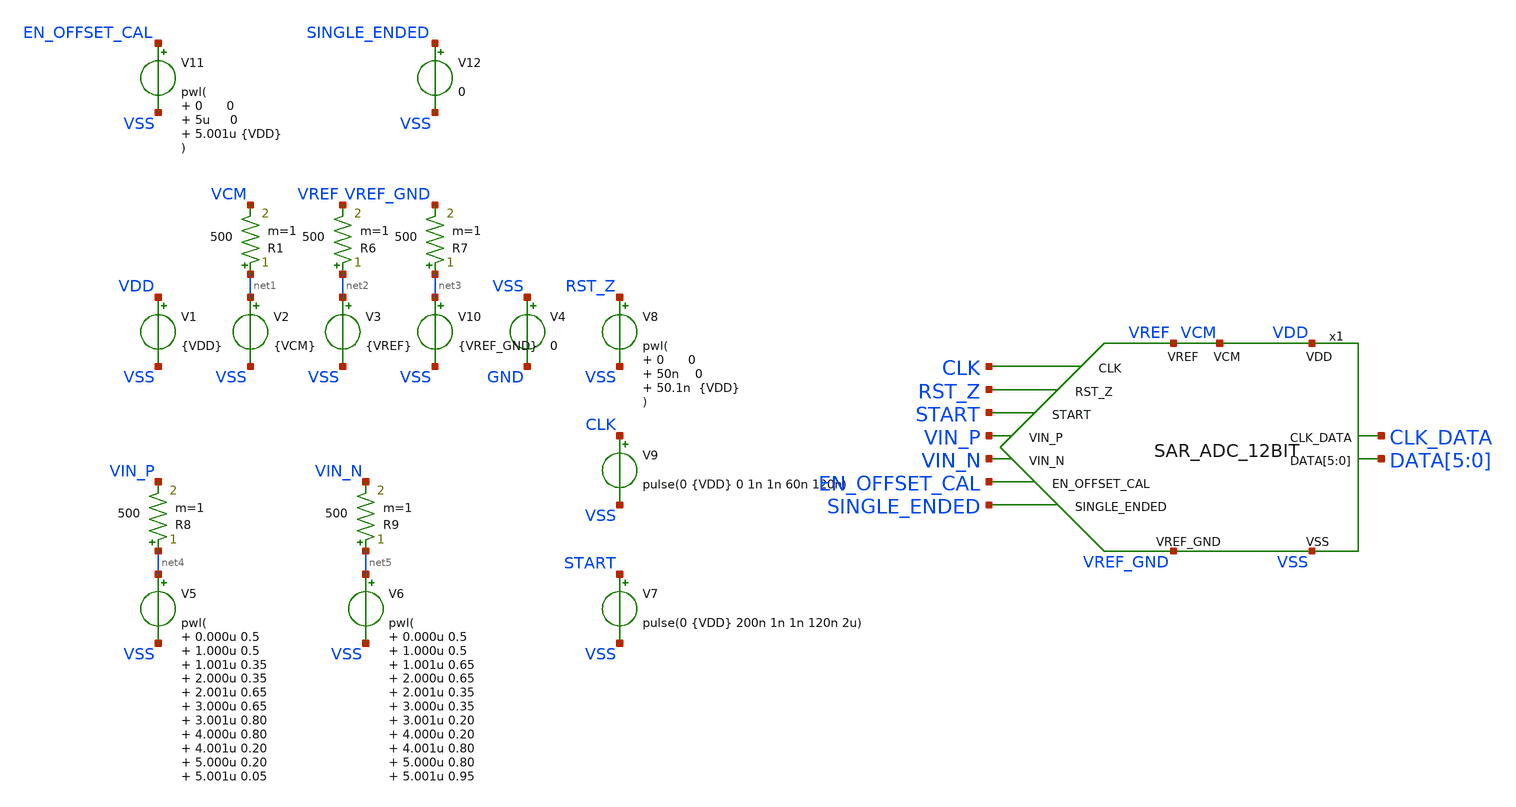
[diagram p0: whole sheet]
** sch_path: schematic/top_level_differential_sim1.sch
* IHP-GmbH/IHP-Open-PDK/ihp-sg13g2/libs.tech/xschem/sg13g2_stdcells/sg13g2_and3_1.sch:
* Copyright 2023 IHP PDK Authors
* Licensed under the Apache License, Version 2.0 (the "License");


* Models for standard digital cells
.include $PDK_ROOT/ihp-sg13g2/libs.ref/sg13g2_stdcell/spice/sg13g2_stdcell.spice

* Spice netlist for state machine generated by openlane
.include $HOME/SAR_ADC_12bit_ihp/schematic/state_machine/state_machine.spice

**.subckt top_level_differential_sim1
x1 VDD VCM VSS VREF VIN_P VIN_N RST_Z CLK_DATA DATA[5] DATA[4] DATA[3] DATA[2] DATA[1] DATA[0] START
+ EN_OFFSET_CAL CLK VREF_GND SINGLE_ENDED SAR_ADC_12BIT
V1 VDD VSS {VDD}
.save i(v1)
V2 net1 VSS {VCM}
.save i(v2)
V3 net2 VSS {VREF}
.save i(v3)
V4 VSS GND 0
V7 START VSS pulse(0 {VDD} 200n 1n 1n 120n 2u)
V8 RST_Z VSS pwl( 0 0 50n 0 50.1n {VDD}
)
V5 net4 VSS pwl( 0.000u 0.5 1.000u 0.5 1.001u 0.35 2.000u 0.35 2.001u 0.65 3.000u 0.65 3.001u 0.80
+ 4.000u 0.80 4.001u 0.20 5.000u 0.20 5.001u 0.05 6.000u 0.05 6.001u 0.95 7.000u 0.95
)
R1 net1 VCM 500 m=1
V9 CLK VSS pulse(0 {VDD} 0 1n 1n 60n 120n)
V6 net5 VSS pwl( 0.000u 0.5 1.000u 0.5 1.001u 0.65 2.000u 0.65 2.001u 0.35 3.000u 0.35 3.001u 0.20
+ 4.000u 0.20 4.001u 0.80 5.000u 0.80 5.001u 0.95 6.000u 0.95 6.001u 0.05 7.000u 0.05
)
V10 net3 VSS {VREF_GND}
.save i(v10)
R6 net2 VREF 500 m=1
R7 net3 VREF_GND 500 m=1
R8 net4 VIN_P 500 m=1
R9 net5 VIN_N 500 m=1
V11 EN_OFFSET_CAL VSS pwl( 0 0 5u 0 5.001u {VDD}
)
V12 SINGLE_ENDED VSS 0
**** begin user architecture code


* Supply, common mode and reference voltage
.param VDD = 1.2
.param VREF = 1
.param VREF_GND = 0
.param VCM = 0.5

.option temp = 27

*.save all

* Control signals
.save start rst_z clk en_offset_cal

* Input signals
.save vin_p vin_n

* Reference, supply
.save vref vref_gnd vcm vdd

* Output signals
.save clk_data data[5] data[4] data[3] data[2] data[1] data[0]

* Internal signals
.save x1.vdac_p x1.vdac_n x1.vdac_pi x1.vdac_ni x1.smpl x1.en_comp x1.comp_p x1.comp_n x1.cal_p x1.cal_n
.save x1.en_vin_bstr_p x1.en_vin_bstr_n
.save x1.c10_p_btm x1.c9_p_btm x1.c8_p_btm x1.c7_p_btm x1.c6_p_btm x1.c5_p_btm x1.c4_p_btm x1.c3_p_btm x1.c2_p_btm x1.c1_p_btm x1.c0_p_btm x1.C0_dummy_p_btm
.save x1.c10_n_btm x1.c9_n_btm x1.c8_n_btm x1.c7_n_btm x1.c6_n_btm x1.c5_n_btm x1.c4_n_btm x1.c3_n_btm x1.c2_n_btm x1.c1_n_btm x1.c0_n_btm x1.C0_dummy_n_btm

.option GMIN=1e-12 reltol=1e-5
.control
		set ngbehavior=hsa
          	set ng_nomodcheck
  		set num_threads=4
  		option noinit
  		option klu
		tran 10n 8u
		write top_level_differential_sim1.raw
.endc


**** end user architecture code
**.ends

* expanding   symbol:  SAR_ADC_12BIT.sym # of pins=14
** sym_path: schematic/SAR_ADC_12BIT.sym
** sch_path: schematic/SAR_ADC_12BIT.sch
.subckt SAR_ADC_12BIT VDD VCM VSS VREF VIN_P VIN_N RST_Z CLK_DATA DATA[5] DATA[4] DATA[3] DATA[2]
+ DATA[1] DATA[0] START EN_OFFSET_CAL CLK VREF_GND SINGLE_ENDED
*.ipin VIN_P
*.ipin VDD
*.ipin VREF
*.ipin VCM
*.ipin VSS
*.ipin VIN_N
*.ipin RST_Z
*.ipin START
*.opin CLK_DATA
*.opin DATA[5],DATA[4],DATA[3],DATA[2],DATA[1],DATA[0]
*.ipin EN_OFFSET_CAL
*.ipin CLK
*.ipin VREF_GND
*.ipin SINGLE_ENDED
x1 VDD VDAC_Pi VDAC_Ni COMP_P EN_COMP COMP_N VSS latched_comparator
x2 VDD COMP_P EN_COMP CAL_P CAL_N EN_VOS_CAL VSS OFFSET_CAL_CYCLE offset_calibration-1
x3 VDAC_N VDAC_P VDD RST_Z VDAC_Pi VDAC_Ni VSS CAL_P CAL_N preamplifier
x4 VCM VREF_GND VREF VIN_P EN_VIN_BSTR_P EN_REF_Z_P[10] EN_REF_Z_P[9] EN_REF_Z_P[8] EN_REF_Z_P[7]
+ EN_REF_Z_P[6] EN_REF_Z_P[5] EN_REF_Z_P[4] EN_REF_Z_P[3] EN_REF_Z_P[2] EN_REF_Z_P[1] EN_REF_Z_P[0] EN_VSS_P[10]
+ EN_VSS_P[9] EN_VSS_P[8] EN_VSS_P[7] EN_VSS_P[6] EN_VSS_P[5] EN_VSS_P[4] EN_VSS_P[3] EN_VSS_P[2] EN_VSS_P[1]
+ EN_VSS_P[0] EN_VCM[10] EN_VCM[9] EN_VCM[8] EN_VCM[7] EN_VCM[6] EN_VCM[5] EN_VCM[4] EN_VCM[3] EN_VCM[2]
+ EN_VCM[1] EN_VCM[0] EN_VCM_SW EN_VCM_DUMMY C8_P_btm C7_P_btm C0_P_btm C6_P_btm C5_P_btm C0_dummy_P_btm
+ C4_P_btm C3_P_btm VDAC_P C10_P_btm C9_P_btm C2_P_btm C1_P_btm VDD VSS switches
x5 VCM VREF_GND VREF VIN_N EN_VIN_BSTR_N EN_REF_Z_N[10] EN_REF_Z_N[9] EN_REF_Z_N[8] EN_REF_Z_N[7]
+ EN_REF_Z_N[6] EN_REF_Z_N[5] EN_REF_Z_N[4] EN_REF_Z_N[3] EN_REF_Z_N[2] EN_REF_Z_N[1] EN_REF_Z_N[0] EN_VSS_N[10]
+ EN_VSS_N[9] EN_VSS_N[8] EN_VSS_N[7] EN_VSS_N[6] EN_VSS_N[5] EN_VSS_N[4] EN_VSS_N[3] EN_VSS_N[2] EN_VSS_N[1]
+ EN_VSS_N[0] EN_VCM[10] EN_VCM[9] EN_VCM[8] EN_VCM[7] EN_VCM[6] EN_VCM[5] EN_VCM[4] EN_VCM[3] EN_VCM[2]
+ EN_VCM[1] EN_VCM[0] EN_VCM_SW EN_VCM_DUMMY C8_N_btm C7_N_btm C0_N_btm C6_N_btm C5_N_btm C0_dummy_N_btm
+ C4_N_btm C3_N_btm VDAC_N C10_N_btm C9_N_btm C2_N_btm C1_N_btm VDD VSS switches
x8 EN_VSS_P_BBM[10] EN_VSS_P_BBM[9] EN_VSS_P_BBM[8] EN_VSS_P_BBM[7] EN_VSS_P_BBM[6] EN_VSS_P_BBM[5]
+ EN_VSS_P_BBM[4] EN_VSS_P_BBM[3] EN_VSS_P_BBM[2] EN_VSS_P_BBM[1] EN_VSS_P_BBM[0] VDD VSS EN_VSS_P[10] EN_VSS_P[9]
+ EN_VSS_P[8] EN_VSS_P[7] EN_VSS_P[6] EN_VSS_P[5] EN_VSS_P[4] EN_VSS_P[3] EN_VSS_P[2] EN_VSS_P[1] EN_VSS_P[0]
+ EN_REF_Z_P[10] EN_REF_Z_P[9] EN_REF_Z_P[8] EN_REF_Z_P[7] EN_REF_Z_P[6] EN_REF_Z_P[5] EN_REF_Z_P[4] EN_REF_Z_P[3]
+ EN_REF_Z_P[2] EN_REF_Z_P[1] EN_REF_Z_P[0] EN_REF_Z_P_BBM[10] EN_REF_Z_P_BBM[9] EN_REF_Z_P_BBM[8]
+ EN_REF_Z_P_BBM[7] EN_REF_Z_P_BBM[6] EN_REF_Z_P_BBM[5] EN_REF_Z_P_BBM[4] EN_REF_Z_P_BBM[3] EN_REF_Z_P_BBM[2]
+ EN_REF_Z_P_BBM[1] EN_REF_Z_P_BBM[0] break_before_make
x9 VDD EN_VIN_BSTR_P VSS SMPL_ON_P VIN_P SMPL bootstrap
x10 VDD EN_VIN_BSTR_N VSS SMPL_ON_N VIN_N SMPL bootstrap
C0_dummy C0_dummy_P_btm VDAC_P 10f m=1
C0 C0_P_btm VDAC_P 10f m=1
C1 C1_P_btm VDAC_P 20f m=1
C2 C2_P_btm VDAC_P 40f m=1
C3 C3_P_btm VDAC_P 80f m=1
C4 C4_P_btm VDAC_P 160f m=1
C5 C5_P_btm VDAC_P 320f m=1
C6 C6_P_btm VDAC_P 640f m=1
C7 C7_P_btm VDAC_P 1.28p m=1
C8 C8_P_btm VDAC_P 2.56p m=1
C9 C9_P_btm VDAC_P 5.12p m=1
C10 C10_P_btm VDAC_P 10.24p m=1
C11 VSS VDAC_P 20.48p m=1
C12 VDAC_N C0_dummy_N_btm 10f m=1
C13 VDAC_N C0_N_btm 10f m=1
C14 VDAC_N C1_N_btm 20f m=1
C15 VDAC_N C2_N_btm 40f m=1
C16 VDAC_N C3_N_btm 80f m=1
C17 VDAC_N C4_N_btm 160f m=1
C18 VDAC_N C5_N_btm 320f m=1
C19 VDAC_N C6_N_btm 640f m=1
C20 VDAC_N C7_N_btm 1.28p m=1
C21 VDAC_N C8_N_btm 2.56p m=1
C22 VDAC_N C9_N_btm 5.12p m=1
C23 VDAC_N C10_N_btm 10.24p m=1
C24 VDAC_N VSS 20.48p m=1
.ends


* expanding   symbol:  latched_comparator/latched_comparator.sym # of pins=7
** sym_path: schematic/latched_comparator/latched_comparator.sym
** sch_path: schematic/latched_comparator/latched_comparator.sch
.subckt latched_comparator VDD Vin_P Vin_N OUT_P EN OUT_N VSS
*.ipin Vin_P
*.ipin Vin_N
*.iopin VDD
*.iopin VSS
*.ipin EN
*.opin OUT_P
*.opin OUT_N
XM1 net1 ENi VDD VDD sg13_lv_pmos w=0.32u l=0.15u ng=1 m=1 mm_ok=1
XM2 OUT_Ni ENi VDD VDD sg13_lv_pmos w=0.32u l=0.15u ng=1 m=1 mm_ok=1
XM3 OUT_Ni OUT_Pi VDD VDD sg13_lv_pmos w=1.25u l=0.15u ng=1 m=1 mm_ok=1
XM4 net2 ENi VDD VDD sg13_lv_pmos w=0.32u l=0.15u ng=1 m=1 mm_ok=1
XM5 OUT_Pi ENi VDD VDD sg13_lv_pmos w=0.32u l=0.15u ng=1 m=1 mm_ok=1
XM6 OUT_Pi OUT_Ni VDD VDD sg13_lv_pmos w=1.25u l=0.15u ng=1 m=1 mm_ok=1
XM7 net1 Vin_P net3 VSS sg13_lv_nmos w=0.55u l=0.13u ng=1 m=1 mm_ok=1
XM8 net2 Vin_N net3 VSS sg13_lv_nmos w=0.55u l=0.13u ng=1 m=1 mm_ok=1
XM9 OUT_Pi OUT_Ni net2 VSS sg13_lv_nmos w=0.42u l=0.15u ng=1 m=1 mm_ok=1
XM10 OUT_Ni OUT_Pi net1 VSS sg13_lv_nmos w=0.42u l=0.15u ng=1 m=1 mm_ok=1
XM11 net3 net3 net3 VSS sg13_lv_nmos w=0.55u l=0.13u ng=1 m=2 mm_ok=1
XM12 net3 ENi VSS VSS sg13_lv_nmos w=0.9u l=0.15u ng=1 m=2 mm_ok=1
x4 net4 OUT_Pi VDD VSS sg13g2_inv_2
x5 net5 OUT_Ni VDD VSS sg13g2_inv_2
x1 ENi EN VDD VSS sg13g2_buf_4
x6 OUT_P net4 VDD VSS sg13g2_inv_4
x2 OUT_N net5 VDD VSS sg13g2_inv_4
.ends


* expanding   symbol:  offset_calibration/offset_calibration-1.sym # of pins=8
** sym_path: schematic/offset_calibration/offset_calibration-1.sym
** sch_path: schematic/offset_calibration/offset_calibration-1.sch
.subckt offset_calibration-1 VDD CAL_RESULT EN_COMP CAL_P CAL_N EN VSS CAL_CYCLE
*.ipin EN_COMP
*.opin CAL_N
*.opin CAL_P
*.ipin VDD
*.ipin VSS
*.ipin EN
*.ipin CAL_RESULT
*.ipin CAL_CYCLE
XM2 CAL_N EN VDD VDD sg13_lv_pmos w=0.225u l=0.35u ng=1 m=1 mm_ok=1
XM1 net6 CAL_RESULT_Z VDD VDD sg13_lv_pmos w=0.225u l=0.35u ng=1 m=1 mm_ok=1
XM3 net5 EN_COMP_Z net6 VDD sg13_lv_pmos w=0.225u l=0.35u ng=1 m=1 mm_ok=1
XM4 CAL_P EN VDD VDD sg13_lv_pmos w=0.225u l=0.35u ng=1 m=1 mm_ok=1
XM5 net3 CAL_RESULTi VDD VDD sg13_lv_pmos w=0.225u l=0.35u ng=1 m=1 mm_ok=1
XM6 net2 EN_COMP_Z net3 VDD sg13_lv_pmos w=0.225u l=0.35u ng=1 m=1 mm_ok=1
XM7 net5 LOAD_CAL_Z CAL_N VDD sg13_lv_pmos w=0.225u l=0.35u ng=1 m=1 mm_ok=1
XM8 net2 LOAD_CAL_Z CAL_P VDD sg13_lv_pmos w=0.225u l=0.35u ng=1 m=1 mm_ok=1
XM9 VDD CAL_N VDD VDD sg13_lv_pmos w=10u l=6.4u ng=3 m=1 mm_ok=1
XM10 VDD CAL_P VDD VDD sg13_lv_pmos w=10u l=6.4u ng=3 m=1 mm_ok=1
XM11 net5 EN_COMPi net4 VSS sg13_lv_nmos w=0.22u l=0.35u ng=1 m=1 mm_ok=1
XM12 net4 CAL_RESULT_Z VSS VSS sg13_lv_nmos w=0.22u l=0.35u ng=1 m=1 mm_ok=1
XM13 net5 LOAD_CALi CAL_N VSS sg13_lv_nmos w=0.22u l=0.35u ng=1 m=1 mm_ok=1
XM14 net2 EN_COMPi net1 VSS sg13_lv_nmos w=0.22u l=0.35u ng=1 m=1 mm_ok=1
XM15 net1 CAL_RESULTi VSS VSS sg13_lv_nmos w=0.22u l=0.35u ng=1 m=1 mm_ok=1
XM16 net2 LOAD_CALi CAL_P VSS sg13_lv_nmos w=0.22u l=0.35u ng=1 m=1 mm_ok=1
x1 CAL_RESULT_Z CAL_RESULT CAL_CYCLE VDD VSS sg13g2_and2_1
x2 EN_COMP_Z EN_COMP CAL_CYCLE VDD VSS sg13g2_and2_1
x3 LOAD_CAL_Z EN net8 net7 VDD VSS sg13g2_and3_1
x4 net8 EN_COMPi VDD VSS sg13g2_inv_1
x5 net7 CAL_CYCLE VDD VSS sg13g2_inv_1
x6 CAL_RESULTi CAL_RESULT_Z VDD VSS sg13g2_inv_1
x7 EN_COMPi EN_COMP_Z VDD VSS sg13g2_inv_1
x8 LOAD_CALi LOAD_CAL_Z VDD VSS sg13g2_inv_1
.ends


* expanding   symbol:  preamplifier/preamplifier.sym # of pins=9
** sym_path: schematic/preamplifier/preamplifier.sym
** sch_path: schematic/preamplifier/preamplifier.sch
.subckt preamplifier IN_N IN_P VDD EN OUT_P OUT_N VSS CAL_P CAL_N
*.ipin VDD
*.ipin VSS
*.ipin IN_P
*.ipin IN_N
*.opin OUT_P
*.opin OUT_N
*.ipin EN
*.ipin CAL_P
*.ipin CAL_N
XM3 net1 net2 VDD VDD sg13_lv_pmos w=1.058u l=1u ng=1 m=6 mm_ok=1
XM2 net2 EN VDD VDD sg13_lv_pmos w=0.305u l=0.15u ng=1 m=1 mm_ok=1
XM5 VDD net2 VDD VDD sg13_lv_pmos w=1.058u l=1u ng=1 m=2 mm_ok=1
XM6 net4 net2 VDD VDD sg13_lv_pmos w=1.058u l=1u ng=1 m=1 mm_ok=1
XM1 net2 net2 VDD VDD sg13_lv_pmos w=1.058u l=1u ng=1 m=1 mm_ok=1
XM4 net8 net2 VDD VDD sg13_lv_pmos w=1.058u l=1u ng=1 m=3 mm_ok=1
XM7 net11 IN_P net1 VDD sg13_lv_pmos w=4.8u l=0.2u ng=2 m=4 mm_ok=1
XM8 net6 IN_N net1 VDD sg13_lv_pmos w=4.8u l=0.2u ng=2 m=4 mm_ok=1
XM9 OUT_P VSS net6 VDD sg13_hv_pmos w=14.6u l=0.4u ng=2 m=1 mm_ok=1
XM10 OUT_N VSS net11 VDD sg13_hv_pmos w=14.6u l=0.4u ng=2 m=1 mm_ok=1
XM11 net9 CAL_P net8 VDD sg13_lv_pmos w=1u l=1.77u ng=1 m=1 mm_ok=1
XM12 net10 CAL_N net8 VDD sg13_lv_pmos w=1u l=1.77u ng=1 m=1 mm_ok=1
XM13 net10 net5 VSS VSS sg13_lv_nmos w=1.118u l=0.15u ng=1 m=1 mm_ok=1
XM14 net9 net5 VSS VSS sg13_lv_nmos w=1.118u l=0.15u ng=1 m=1 mm_ok=1
XM15 net9 VSS VSS VSS sg13_lv_nmos w=1.118u l=0.15u ng=1 m=1 mm_ok=1
XM16 net10 VSS VSS VSS sg13_lv_nmos w=1.118u l=0.15u ng=1 m=1 mm_ok=1
XM17 net3 net3 VSS VSS sg13_lv_nmos w=0.9u l=0.15u ng=1 m=1 mm_ok=1
XM18 net5 net3 VSS VSS sg13_lv_nmos w=0.9u l=0.15u ng=1 m=2 mm_ok=1
XM19 VSS net3 VSS VSS sg13_lv_nmos w=0.9u l=0.15u ng=1 m=2 mm_ok=1
x1 EN_Z EN VDD VSS sg13g2_inv_1
XM20 OUT_P net4 net10 VSS sg13_lv_nmos w=0.9u l=0.15u ng=1 m=4 mm_ok=1
XM21 OUT_N net4 net9 VSS sg13_lv_nmos w=0.9u l=0.15u ng=1 m=4 mm_ok=1
XM22 net7 EN VSS VSS sg13_lv_nmos w=3.5u l=0.15u ng=1 m=1 mm_ok=1
XM23 net4 EN_Z VSS VSS sg13_lv_nmos w=0.42u l=0.15u ng=1 m=1 mm_ok=1
XM24 VDD OUT_N net5 VSS sg13_hv_nmos w=0.69u l=0.5u ng=1 m=1 rfmode=1 mm_ok=1
XM25 VDD OUT_P net5 VSS sg13_hv_nmos w=0.69u l=0.5u ng=1 m=1 rfmode=1 mm_ok=1
XR3 OUT_N rn[0] gnd rhigh w=0.5e-6 l=2.75e-6 m=1 b=0 mm_ok=1
XR1 rp[0] OUT_P gnd rhigh w=0.5e-6 l=2.75e-6 m=1 b=0 mm_ok=1
XR2 net14 net7 gnd rhigh w=0.5e-6 l=2.75e-6 m=1 b=0 mm_ok=1
XR4 net13 net14 gnd rhigh w=0.5e-6 l=2.75e-6 m=1 b=0 mm_ok=1
XR5 net12 net13 gnd rhigh w=0.5e-6 l=2.75e-6 m=1 b=0 mm_ok=1
XR6 net2 net12 gnd rhigh w=0.5e-6 l=2.75e-6 m=1 b=0 mm_ok=1
XR7 net15 net3 gnd rhigh w=0.5e-6 l=2.75e-6 m=1 b=0 mm_ok=1
XR8 net4 net15 gnd rhigh w=0.5e-6 l=2.75e-6 m=1 b=0 mm_ok=1
.ends


* expanding   symbol:  switches/switches.sym # of pins=25
** sym_path: schematic/switches/switches.sym
** sch_path: schematic/switches/switches.sch
.subckt switches VCM VREF_GND VREF VIN EN_VIN EN_VREF_Z[10] EN_VREF_Z[9] EN_VREF_Z[8] EN_VREF_Z[7]
+ EN_VREF_Z[6] EN_VREF_Z[5] EN_VREF_Z[4] EN_VREF_Z[3] EN_VREF_Z[2] EN_VREF_Z[1] EN_VREF_Z[0] EN_VSS[10] EN_VSS[9]
+ EN_VSS[8] EN_VSS[7] EN_VSS[6] EN_VSS[5] EN_VSS[4] EN_VSS[3] EN_VSS[2] EN_VSS[1] EN_VSS[0] EN_VCM[10]
+ EN_VCM[9] EN_VCM[8] EN_VCM[7] EN_VCM[6] EN_VCM[5] EN_VCM[4] EN_VCM[3] EN_VCM[2] EN_VCM[1] EN_VCM[0] EN_VCM_SW
+ EN_VCM_DUMMY Cbtm_8 Cbtm_7 Cbtm_0 Cbtm_6 Cbtm_5 Cbtm_0_dummy Cbtm_4 Cbtm_3 VDAC Cbtm_10 Cbtm_9 Cbtm_2 Cbtm_1 VDD
+ VSS
*.ipin VCM
*.ipin VREF_GND
*.ipin VREF
*.ipin VIN
*.ipin VDD
*.opin Cbtm_0_dummy
*.opin Cbtm_0
*.opin Cbtm_1
*.opin Cbtm_2
*.opin Cbtm_3
*.opin Cbtm_4
*.opin Cbtm_5
*.opin Cbtm_6
*.opin Cbtm_7
*.opin Cbtm_8
*.opin Cbtm_9
*.opin Cbtm_10
*.opin VDAC
*.ipin EN_VIN
*.ipin
*+ EN_VREF_Z[10],EN_VREF_Z[9],EN_VREF_Z[8],EN_VREF_Z[7],EN_VREF_Z[6],EN_VREF_Z[5],EN_VREF_Z[4],EN_VREF_Z[3],EN_VREF_Z[2],EN_VREF_Z[1],EN_VREF_Z[0]
*.ipin
*+ EN_VSS[10],EN_VSS[9],EN_VSS[8],EN_VSS[7],EN_VSS[6],EN_VSS[5],EN_VSS[4],EN_VSS[3],EN_VSS[2],EN_VSS[1],EN_VSS[0]
*.ipin
*+ EN_VCM[10],EN_VCM[9],EN_VCM[8],EN_VCM[7],EN_VCM[6],EN_VCM[5],EN_VCM[4],EN_VCM[3],EN_VCM[2],EN_VCM[1],EN_VCM[0]
*.ipin EN_VCM_DUMMY
*.ipin EN_VCM_SW
*.ipin VSS
x1 VCM VIN EN_VCM_DUMMY Cbtm_0_dummy EN_VIN VSS switch_C0_dummy
e VCM VREF_GND VIN VREF EN_VCM[0] EN_VREF_Z[0] Cbtm_0 VDD EN_VSS[0] EN_VIN VSS switch_C5
x3 VCM VREF_GND VIN VREF EN_VCM[1] EN_VREF_Z[1] Cbtm_1 VDD EN_VSS[1] EN_VIN VSS switch_C5
x4 VCM VREF_GND VIN VREF EN_VCM[2] EN_VREF_Z[2] Cbtm_2 VDD EN_VSS[2] EN_VIN VSS switch_C5
x5 VCM VREF_GND VIN VREF EN_VCM[3] EN_VREF_Z[3] Cbtm_3 VDD EN_VSS[3] EN_VIN VSS switch_C5
x6 VCM VREF_GND VIN VREF EN_VCM[4] EN_VREF_Z[4] Cbtm_4 VDD EN_VSS[4] EN_VIN VSS switch_C5
x7 VCM VREF_GND VIN VREF EN_VCM[5] EN_VREF_Z[5] Cbtm_5 VDD EN_VSS[5] EN_VIN VSS switch_C5
x8 VCM VREF_GND VIN VREF EN_VCM[6] EN_VREF_Z[6] Cbtm_6 VDD EN_VSS[6] EN_VIN VSS switch_C6
x9 VCM VREF_GND VIN VREF EN_VCM[7] EN_VREF_Z[7] Cbtm_7 VDD EN_VSS[7] EN_VIN VSS switch_C7
x10 VCM VREF_GND VIN VREF EN_VCM[8] EN_VREF_Z[8] Cbtm_8 VDD EN_VSS[8] EN_VIN VSS switch_C8
x11 VCM VREF_GND VIN VREF EN_VCM[9] EN_VREF_Z[9] Cbtm_9 VDD EN_VSS[9] EN_VIN VSS switch_C9
x12 VCM VREF_GND VIN VREF EN_VCM[10] EN_VREF_Z[10] Cbtm_10 VDD EN_VSS[10] EN_VIN VSS switch_C10
x13 VCM EN_VCM_SW VDAC VDD VSS switch_VCM
.ends


* expanding   symbol:  break_before_make/break_before_make.sym # of pins=6
** sym_path: schematic/break_before_make/break_before_make.sym
** sch_path: schematic/break_before_make/break_before_make.sch
.subckt break_before_make EN_VSS_I[10] EN_VSS_I[9] EN_VSS_I[8] EN_VSS_I[7] EN_VSS_I[6] EN_VSS_I[5]
+ EN_VSS_I[4] EN_VSS_I[3] EN_VSS_I[2] EN_VSS_I[1] EN_VSS_I[0] VDD VSS EN_VSS_O[10] EN_VSS_O[9] EN_VSS_O[8]
+ EN_VSS_O[7] EN_VSS_O[6] EN_VSS_O[5] EN_VSS_O[4] EN_VSS_O[3] EN_VSS_O[2] EN_VSS_O[1] EN_VSS_O[0] EN_VREF_Z_O[10]
+ EN_VREF_Z_O[9] EN_VREF_Z_O[8] EN_VREF_Z_O[7] EN_VREF_Z_O[6] EN_VREF_Z_O[5] EN_VREF_Z_O[4] EN_VREF_Z_O[3]
+ EN_VREF_Z_O[2] EN_VREF_Z_O[1] EN_VREF_Z_O[0] EN_VREF_Z_I[10] EN_VREF_Z_I[9] EN_VREF_Z_I[8] EN_VREF_Z_I[7]
+ EN_VREF_Z_I[6] EN_VREF_Z_I[5] EN_VREF_Z_I[4] EN_VREF_Z_I[3] EN_VREF_Z_I[2] EN_VREF_Z_I[1] EN_VREF_Z_I[0]
*.ipin
*+ EN_VSS_I[10],EN_VSS_I[9],EN_VSS_I[8],EN_VSS_I[7],EN_VSS_I[6],EN_VSS_I[5],EN_VSS_I[4],EN_VSS_I[3],EN_VSS_I[2],EN_VSS_I[1],EN_VSS_I[0]
*.ipin
*+ EN_VREF_Z_I[10],EN_VREF_Z_I[9],EN_VREF_Z_I[8],EN_VREF_Z_I[7],EN_VREF_Z_I[6],EN_VREF_Z_I[5],EN_VREF_Z_I[4],EN_VREF_Z_I[3],EN_VREF_Z_I[2],EN_VREF_Z_I[1],EN_VREF_Z_I[0]
*.ipin VDD
*.ipin VSS
*.opin
*+ EN_VSS_O[10],EN_VSS_O[9],EN_VSS_O[8],EN_VSS_O[7],EN_VSS_O[6],EN_VSS_O[5],EN_VSS_O[4],EN_VSS_O[3],EN_VSS_O[2],EN_VSS_O[1],EN_VSS_O[0]
*.opin
*+ EN_VREF_Z_O[10],EN_VREF_Z_O[9],EN_VREF_Z_O[8],EN_VREF_Z_O[7],EN_VREF_Z_O[6],EN_VREF_Z_O[5],EN_VREF_Z_O[4],EN_VREF_Z_O[3],EN_VREF_Z_O[2],EN_VREF_Z_O[1],EN_VREF_Z_O[0]
x1[10] EN_VSS_O[10] EN_VSS_I[10] EN_VREF_Z_O[10] VDD VSS sg13g2_and2_2
x1[9] EN_VSS_O[9] EN_VSS_I[9] EN_VREF_Z_O[9] VDD VSS sg13g2_and2_2
x1[8] EN_VSS_O[8] EN_VSS_I[8] EN_VREF_Z_O[8] VDD VSS sg13g2_and2_2
x1[7] EN_VSS_O[7] EN_VSS_I[7] EN_VREF_Z_O[7] VDD VSS sg13g2_and2_2
x1[6] EN_VSS_O[6] EN_VSS_I[6] EN_VREF_Z_O[6] VDD VSS sg13g2_and2_2
x1[5] EN_VSS_O[5] EN_VSS_I[5] EN_VREF_Z_O[5] VDD VSS sg13g2_and2_2
x1[4] EN_VSS_O[4] EN_VSS_I[4] EN_VREF_Z_O[4] VDD VSS sg13g2_and2_2
x1[3] EN_VSS_O[3] EN_VSS_I[3] EN_VREF_Z_O[3] VDD VSS sg13g2_and2_2
x1[2] EN_VSS_O[2] EN_VSS_I[2] EN_VREF_Z_O[2] VDD VSS sg13g2_and2_2
x1[1] EN_VSS_O[1] EN_VSS_I[1] EN_VREF_Z_O[1] VDD VSS sg13g2_and2_2
x1[0] EN_VSS_O[0] EN_VSS_I[0] EN_VREF_Z_O[0] VDD VSS sg13g2_and2_2
x2[10] EN_VREF_Z_O[10] EN_VSS_O[10] EN_VREF_Z_I[10] VDD VSS sg13g2_or2_2
x2[9] EN_VREF_Z_O[9] EN_VSS_O[9] EN_VREF_Z_I[9] VDD VSS sg13g2_or2_2
x2[8] EN_VREF_Z_O[8] EN_VSS_O[8] EN_VREF_Z_I[8] VDD VSS sg13g2_or2_2
x2[7] EN_VREF_Z_O[7] EN_VSS_O[7] EN_VREF_Z_I[7] VDD VSS sg13g2_or2_2
x2[6] EN_VREF_Z_O[6] EN_VSS_O[6] EN_VREF_Z_I[6] VDD VSS sg13g2_or2_2
x2[5] EN_VREF_Z_O[5] EN_VSS_O[5] EN_VREF_Z_I[5] VDD VSS sg13g2_or2_2
x2[4] EN_VREF_Z_O[4] EN_VSS_O[4] EN_VREF_Z_I[4] VDD VSS sg13g2_or2_2
x2[3] EN_VREF_Z_O[3] EN_VSS_O[3] EN_VREF_Z_I[3] VDD VSS sg13g2_or2_2
x2[2] EN_VREF_Z_O[2] EN_VSS_O[2] EN_VREF_Z_I[2] VDD VSS sg13g2_or2_2
x2[1] EN_VREF_Z_O[1] EN_VSS_O[1] EN_VREF_Z_I[1] VDD VSS sg13g2_or2_2
x2[0] EN_VREF_Z_O[0] EN_VSS_O[0] EN_VREF_Z_I[0] VDD VSS sg13g2_or2_2
x1 VDD VSS sg13g2_decap_4
x2 VDD VSS sg13g2_decap_8
.ends


* expanding   symbol:  bootstrap/bootstrap.sym # of pins=6
** sym_path: schematic/bootstrap/bootstrap.sym
** sch_path: schematic/bootstrap/bootstrap.sch
.subckt bootstrap VDD VGATE VSS SW_ON VIN EN
*.ipin VDD
*.ipin VSS
*.ipin VIN
*.ipin EN
*.opin VGATE
*.opin SW_ON
XM5 VDD VGATE Vtop Vtop sg13_lv_pmos w=0.32u l=0.15u ng=1 m=1 mm_ok=1
XM1 VGATE EN_Z_LVL_SHFT Vtop Vtop sg13_lv_pmos w=16u l=0.38u ng=4 m=1 mm_ok=1
XM2 Vtop Vbottom Vtop Vtop sg13_lv_pmos w=10u l=10u ng=2 m=1 mm_ok=1
XM6 EN_Z_LVL_SHFT EN VDD VDD sg13_lv_pmos w=0.35u l=0.15u ng=1 m=1 mm_ok=1
XM7 EN_Z_LVL_SHFT EN Vbottom VSS sg13_lv_nmos w=0.63u l=0.15u ng=1 m=1 mm_ok=1
XM8 EN_Z_LVL_SHFT VGATE Vbottom VSS sg13_lv_nmos w=1.8u l=0.15u ng=2 m=1 mm_ok=1
XM3 Vbottom EN_Z VSS VSS sg13_lv_nmos w=3.5u l=0.15u ng=1 m=1 mm_ok=1
XM10 VIN VGATE Vbottom VSS sg13_lv_nmos w=3.5u l=0.15u ng=1 m=1 mm_ok=1
XM4 net2 EN_Z VSS VSS sg13_lv_nmos w=3.5u l=0.15u ng=1 m=1 mm_ok=1
XM11 VGATE VDD VGATE_1V8 VSS sg13_lv_nmos w=3.5u l=0.45u ng=1 m=1 mm_ok=1
XM9 VGATE VDD net2 VSS sg13_hv_nmos w=6.3u l=0.45u ng=2 m=1 mm_ok=1
x2 SW_ON net1 VDD VSS sg13g2_inv_2
x4 net1 VGATE_1V8 VDD VSS sg13g2_inv_1
x1 EN_Z EN VDD VSS sg13g2_inv_1
.ends


* expanding   symbol:  sg13g2_stdcells/sg13g2_inv_2.sym # of pins=2
** sym_path: sg13g2_stdcells/sg13g2_inv_2.sym
** sch_path: sg13g2_stdcells/sg13g2_inv_2.sch
.subckt sg13g2_inv_2 Y A VDD VSS
*.opin Y
*.ipin A
*.iopin VDD
*.iopin VSS
XM1 Y A VSS VSS sg13_lv_nmos w=1.48u l=130.00n ng=2 m=1 mm_ok=1
XM2 Y A VDD VDD sg13_lv_pmos w=2.24u l=130.00n ng=2 m=1 mm_ok=1
.ends


* expanding   symbol:  sg13g2_stdcells/sg13g2_buf_4.sym # of pins=2
** sym_path: sg13g2_stdcells/sg13g2_buf_4.sym
** sch_path: sg13g2_stdcells/sg13g2_buf_4.sch
.subckt sg13g2_buf_4 X A VDD VSS
*.ipin A
*.opin X
*.iopin VDD
*.iopin VSS
XM1 net1 A VSS VSS sg13_lv_nmos w=740.00n l=130.00n ng=1 m=1 mm_ok=1
XM2 X net1 VSS VSS sg13_lv_nmos w=2.96u l=130.00n ng=4 m=1 mm_ok=1
XM3 net1 A VDD VDD sg13_lv_pmos w=1.68u l=130.00n ng=2 m=1 mm_ok=1
XM4 X net1 VDD VDD sg13_lv_pmos w=4.48u l=130.00n ng=4 m=1 mm_ok=1
.ends


* expanding   symbol:  sg13g2_stdcells/sg13g2_inv_4.sym # of pins=2
** sym_path: sg13g2_stdcells/sg13g2_inv_4.sym
** sch_path: sg13g2_stdcells/sg13g2_inv_4.sch
.subckt sg13g2_inv_4 Y A VDD VSS
*.ipin A
*.opin Y
*.iopin VDD
*.iopin VSS
XM1 Y A VSS VSS sg13_lv_nmos w=2.96u l=130.00n ng=4 m=1 mm_ok=1
XM2 Y A VDD VDD sg13_lv_pmos w=4.48u l=130.00n ng=4 m=1 mm_ok=1
.ends


* expanding   symbol:  sg13g2_stdcells/sg13g2_and2_1.sym # of pins=3
** sym_path: sg13g2_stdcells/sg13g2_and2_1.sym
** sch_path: sg13g2_stdcells/sg13g2_and2_1.sch
.subckt sg13g2_and2_1 X A B VDD VSS
*.ipin A
*.ipin B
*.opin X
*.iopin VDD
*.iopin VSS
XM1 net1 A net2 VSS sg13_lv_nmos w=640.00n l=130.00n ng=1 m=1 mm_ok=1
XM2 net2 B VSS VSS sg13_lv_nmos w=640.00n l=130.00n ng=1 m=1 mm_ok=1
XM3 X net1 VSS VSS sg13_lv_nmos w=740.00n l=130.00n ng=1 m=1 mm_ok=1
XM4 net1 B VDD VDD sg13_lv_pmos w=840.00n l=130.00n ng=1 m=1 mm_ok=1
XM5 net1 A VDD VDD sg13_lv_pmos w=840.00n l=130.00n ng=1 m=1 mm_ok=1
XM6 X net1 VDD VDD sg13_lv_pmos w=1.12u l=130.00n ng=1 m=1 mm_ok=1
.ends


* expanding   symbol:  sg13g2_stdcells/sg13g2_and3_1.sym # of pins=4
** sym_path: sg13g2_stdcells/sg13g2_and3_1.sym
** sch_path: sg13g2_stdcells/sg13g2_and3_1.sch
.subckt sg13g2_and3_1 X A B C VDD VSS
*.opin X
*.ipin C
*.ipin B
*.ipin A
*.iopin VDD
*.iopin VSS
XM1 net2 A net3 VSS sg13_lv_nmos w=640.00n l=130.00n ng=1 m=1 mm_ok=1
XM2 net3 B net1 VSS sg13_lv_nmos w=640.00n l=130.00n ng=1 m=1 mm_ok=1
XM3 net1 C VSS VSS sg13_lv_nmos w=640.00n l=130.00n ng=1 m=1 mm_ok=1
XM4 X net2 VSS VSS sg13_lv_nmos w=740.00n l=130.00n ng=1 m=1 mm_ok=1
XM5 net2 C VDD VDD sg13_lv_pmos w=840.00n l=130.00n ng=1 m=1 mm_ok=1
XM6 net2 B VDD VDD sg13_lv_pmos w=840.00n l=130.00n ng=1 m=1 mm_ok=1
XM7 net2 A VDD VDD sg13_lv_pmos w=840.00n l=130.00n ng=1 m=1 mm_ok=1
XM8 X net2 VDD VDD sg13_lv_pmos w=1.12u l=130.00n ng=1 m=1 mm_ok=1
.ends


* expanding   symbol:  sg13g2_stdcells/sg13g2_inv_1.sym # of pins=2
** sym_path: sg13g2_stdcells/sg13g2_inv_1.sym
** sch_path: sg13g2_stdcells/sg13g2_inv_1.sch
.subckt sg13g2_inv_1 Y A VDD VSS
*.opin Y
*.ipin A
*.iopin VDD
*.iopin VSS
XM1 Y A VSS VSS sg13_lv_nmos w=740.00n l=130.00n ng=1 m=1 mm_ok=1
XM2 Y A VDD VDD sg13_lv_pmos w=1.12u l=130.00n ng=1 m=1 mm_ok=1
.ends


* expanding   symbol:  individual_switches/switch_C0_dummy.sym # of pins=6
** sym_path: schematic/individual_switches/switch_C0_dummy.sym
** sch_path: schematic/individual_switches/switch_C0_dummy.sch
.subckt switch_C0_dummy VCM VIN EN_VCM Cbtm EN_VIN VSS
*.ipin VIN
*.ipin EN_VIN
*.ipin VCM
*.ipin EN_VCM
*.opin Cbtm
*.iopin VSS
XM7 VIN EN_VIN Cbtm VSS sg13_lv_nmos w=0.55u l=0.13u ng=1 m=1 mm_ok=1
XM1 VCM EN_VCM Cbtm VSS sg13_lv_nmos w=1.15u l=0.13u ng=1 m=1 mm_ok=1
.ends


* expanding   symbol:  individual_switches/switch_C5.sym # of pins=11
** sym_path: schematic/individual_switches/switch_C5.sym
** sch_path: schematic/individual_switches/switch_C5.sch
.subckt switch_C5 VCM VREF_GND VIN VREF EN_VCM EN_VREF_Z Cbtm VDD EN_VSS EN_VIN VSS
*.ipin VIN
*.ipin EN_VIN
*.ipin VREF_GND
*.ipin EN_VSS
*.opin Cbtm
*.iopin VSS
*.ipin VREF
*.ipin EN_VREF_Z
*.ipin EN_VCM
*.ipin VCM
*.iopin VDD
XM7 VIN EN_VIN Cbtm VSS sg13_lv_nmos w=0.55u l=0.13u ng=1 m=1 mm_ok=1
XM1 VCM EN_VCM Cbtm VSS sg13_lv_nmos w=1.15u l=0.13u ng=1 m=1 mm_ok=1
XM2 Cbtm EN_VREF_Z VREF VDD sg13_lv_pmos w=0.35u l=0.35u ng=1 m=1 mm_ok=1
XM4 VREF_GND EN_VSS Cbtm VSS sg13_lv_nmos w=0.88u l=0.13u ng=1 m=1 mm_ok=1
.ends


* expanding   symbol:  individual_switches/switch_C6.sym # of pins=11
** sym_path: schematic/individual_switches/switch_C6.sym
** sch_path: schematic/individual_switches/switch_C6.sch
.subckt switch_C6 VCM VREF_GND VIN VREF EN_VCM EN_VREF_Z Cbtm VDD EN_VSS EN_VIN VSS
*.ipin VIN
*.ipin EN_VIN
*.ipin VREF_GND
*.ipin EN_VSS
*.opin Cbtm
*.iopin VSS
*.ipin VREF
*.ipin EN_VREF_Z
*.ipin EN_VCM
*.ipin VCM
*.iopin VDD
XM7 VIN EN_VIN Cbtm VSS sg13_lv_nmos w=0.55u l=0.13u ng=1 m=1 mm_ok=1
XM1 VREF_GND EN_VSS Cbtm VSS sg13_lv_nmos w=1.75u l=0.13u ng=1 m=1 mm_ok=1
XM2 Cbtm EN_VREF_Z VREF VDD sg13_lv_pmos w=8u l=0.35u ng=1 m=1 mm_ok=1
XM3 VCM EN_VCM Cbtm VSS sg13_lv_nmos w=2.3u l=0.13u ng=1 m=1 mm_ok=1
.ends


* expanding   symbol:  individual_switches/switch_C7.sym # of pins=11
** sym_path: schematic/individual_switches/switch_C7.sym
** sch_path: schematic/individual_switches/switch_C7.sch
.subckt switch_C7 VCM VREF_GND VIN VREF EN_VCM EN_VREF_Z Cbtm VDD EN_VSS EN_VIN VSS
*.ipin VIN
*.ipin EN_VIN
*.ipin VREF_GND
*.ipin EN_VSS
*.opin Cbtm
*.iopin VSS
*.ipin VREF
*.ipin EN_VREF_Z
*.ipin EN_VCM
*.ipin VCM
*.iopin VDD
XM4 VIN EN_VIN Cbtm VSS sg13_lv_nmos w=0.9u l=0.13u ng=1 m=1 mm_ok=1
XM1 VREF_GND EN_VSS Cbtm VSS sg13_lv_nmos w=3.45u l=0.13u ng=1 m=1 mm_ok=1
XM2 Cbtm EN_VREF_Z VREF VDD sg13_lv_pmos w=16u l=0.35u ng=2 m=1 mm_ok=1
XM3 VCM EN_VCM Cbtm VSS sg13_lv_nmos w=4.5u l=0.13u ng=1 m=1 mm_ok=1
.ends


* expanding   symbol:  individual_switches/switch_C8.sym # of pins=11
** sym_path: schematic/individual_switches/switch_C8.sym
** sch_path: schematic/individual_switches/switch_C8.sch
.subckt switch_C8 VCM VREF_GND VIN VREF EN_VCM EN_VREF_Z Cbtm VDD EN_VSS EN_VIN VSS
*.ipin VIN
*.ipin EN_VIN
*.ipin VREF_GND
*.ipin EN_VSS
*.opin Cbtm
*.iopin VSS
*.ipin VREF
*.ipin EN_VREF_Z
*.ipin EN_VCM
*.ipin VCM
*.iopin VDD
XM5 VIN EN_VIN Cbtm VSS sg13_lv_nmos w=0.9u l=0.13u ng=1 m=1 mm_ok=1
XM4 VREF_GND EN_VSS Cbtm VSS sg13_lv_nmos w=6.5u l=0.13u ng=1 m=1 mm_ok=1
XM1 Cbtm EN_VREF_Z VREF VDD sg13_lv_pmos w=32u l=0.35u ng=4 m=1 mm_ok=1
XM2 VCM EN_VCM Cbtm VSS sg13_lv_nmos w=8.5u l=0.13u ng=1 m=1 mm_ok=1
.ends


* expanding   symbol:  individual_switches/switch_C9.sym # of pins=11
** sym_path: schematic/individual_switches/switch_C9.sym
** sch_path: schematic/individual_switches/switch_C9.sch
.subckt switch_C9 VCM VREF_GND VIN VREF EN_VCM EN_VREF_Z Cbtm VDD EN_VSS EN_VIN VSS
*.ipin VIN
*.ipin EN_VIN
*.ipin VREF_GND
*.ipin EN_VSS
*.opin Cbtm
*.iopin VSS
*.ipin VREF
*.ipin EN_VREF_Z
*.ipin EN_VCM
*.ipin VCM
*.iopin VDD
XM3 VIN EN_VIN Cbtm VSS sg13_lv_nmos w=0.9u l=0.13u ng=1 m=1 mm_ok=1
XM5 VREF_GND EN_VSS Cbtm VSS sg13_lv_nmos w=13.1u l=0.13u ng=2 m=1 mm_ok=1
XM1 Cbtm EN_VREF_Z VREF VDD sg13_lv_pmos w=64u l=0.35u ng=8 m=1 mm_ok=1
XM2 VCM EN_VCM Cbtm VSS sg13_lv_nmos w=17u l=0.13u ng=2 m=1 mm_ok=1
.ends


* expanding   symbol:  individual_switches/switch_C10.sym # of pins=11
** sym_path: schematic/individual_switches/switch_C10.sym
** sch_path: schematic/individual_switches/switch_C10.sch
.subckt switch_C10 VCM VREF_GND VIN VREF EN_VCM EN_VREF_Z Cbtm VDD EN_VSS EN_VIN VSS
*.ipin VIN
*.ipin EN_VIN
*.ipin VREF_GND
*.ipin EN_VSS
*.opin Cbtm
*.iopin VSS
*.ipin VREF
*.ipin EN_VREF_Z
*.ipin EN_VCM
*.ipin VCM
*.iopin VDD
XM5 VIN EN_VIN Cbtm VSS sg13_lv_nmos w=6.8u l=0.13u ng=2 m=1 mm_ok=1
XM1 VREF_GND EN_VSS Cbtm VSS sg13_lv_nmos w=26u l=0.13u ng=4 m=1 mm_ok=1
XM2 Cbtm EN_VREF_Z VREF VDD sg13_lv_pmos w=128u l=0.35u ng=16 m=1 mm_ok=1
XM3 VCM EN_VCM Cbtm VSS sg13_lv_nmos w=34u l=0.13u ng=4 m=1 mm_ok=1
.ends


* expanding   symbol:  individual_switches/switch_VCM.sym # of pins=5
** sym_path: schematic/individual_switches/switch_VCM.sym
** sch_path: schematic/individual_switches/switch_VCM.sch
.subckt switch_VCM VCM EN_VCM Cbtm VDD VSS
*.ipin VCM
*.ipin EN_VCM
*.opin Cbtm
*.iopin VSS
*.iopin VDD
XM3 VCM EN_VCM Cbtm VSS sg13_lv_nmos w=34u l=0.13u ng=4 m=1 mm_ok=1
.ends


* expanding   symbol:  sg13g2_stdcells/sg13g2_and2_2.sym # of pins=3
** sym_path: sg13g2_stdcells/sg13g2_and2_2.sym
** sch_path: sg13g2_stdcells/sg13g2_and2_2.sch
.subckt sg13g2_and2_2 X A B VDD VSS
*.ipin A
*.ipin B
*.opin X
*.iopin VDD
*.iopin VSS
XM1 net1 A net2 VSS sg13_lv_nmos w=640.00n l=130.00n ng=1 m=1 mm_ok=1
XM2 net2 B VSS VSS sg13_lv_nmos w=640.00n l=130.00n ng=1 m=1 mm_ok=1
XM3 X net1 VSS VSS sg13_lv_nmos w=1.48u l=130.00n ng=2 m=1 mm_ok=1
XM4 net1 B VDD VDD sg13_lv_pmos w=840.00n l=130.00n ng=1 m=1 mm_ok=1
XM5 net1 A VDD VDD sg13_lv_pmos w=840.00n l=130.00n ng=1 m=1 mm_ok=1
XM6 X net1 VDD VDD sg13_lv_pmos w=2.24u l=130.00n ng=2 m=1 mm_ok=1
.ends


* expanding   symbol:  sg13g2_stdcells/sg13g2_or2_2.sym # of pins=3
** sym_path: sg13g2_stdcells/sg13g2_or2_2.sym
** sch_path: sg13g2_stdcells/sg13g2_or2_2.sch
.subckt sg13g2_or2_2 X A B VDD VSS
*.opin X
*.ipin B
*.ipin A
*.iopin VDD
*.iopin VSS
XM1 net1 B VSS VSS sg13_lv_nmos w=550.00n l=130.00n ng=1 m=1 mm_ok=1
XM2 net1 A VSS VSS sg13_lv_nmos w=550.00n l=130.00n ng=1 m=1 mm_ok=1
XM3 X net1 VSS VSS sg13_lv_nmos w=1.48u l=130.00n ng=2 m=1 mm_ok=1
XM4 net2 A VDD VDD sg13_lv_pmos w=840.00n l=130.00n ng=1 m=1 mm_ok=1
XM5 net1 B net2 VDD sg13_lv_pmos w=840.00n l=130.00n ng=1 m=1 mm_ok=1
XM6 X net1 VDD VDD sg13_lv_pmos w=2.24u l=130.00n ng=2 m=1 mm_ok=1
.ends


* expanding   symbol:  sg13g2_stdcells/sg13g2_decap_4.sym # of pins=0
** sym_path: sg13g2_stdcells/sg13g2_decap_4.sym
** sch_path: sg13g2_stdcells/sg13g2_decap_4.sch
.subckt sg13g2_decap_4 VDD VSS
*.iopin VDD
*.iopin VSS
XM1 VSS VDD VSS VSS sg13_lv_nmos w=420.00n l=1.000u ng=1 m=1 mm_ok=1
XM2 VDD VSS VDD VDD sg13_lv_pmos w=1.000u l=1.000u ng=1 m=1 mm_ok=1
.ends


* expanding   symbol:  sg13g2_stdcells/sg13g2_decap_8.sym # of pins=0
** sym_path: sg13g2_stdcells/sg13g2_decap_8.sym
** sch_path: sg13g2_stdcells/sg13g2_decap_8.sch
.subckt sg13g2_decap_8 VDD VSS
*.iopin VDD
*.iopin VSS
XM1 VSS VDD VSS VSS sg13_lv_nmos w=840.00n l=1.000u ng=2 m=1 mm_ok=1
XM2 VDD VSS VDD VDD sg13_lv_pmos w=2.000u l=1.000u ng=2 m=1 mm_ok=1
.ends

.end
